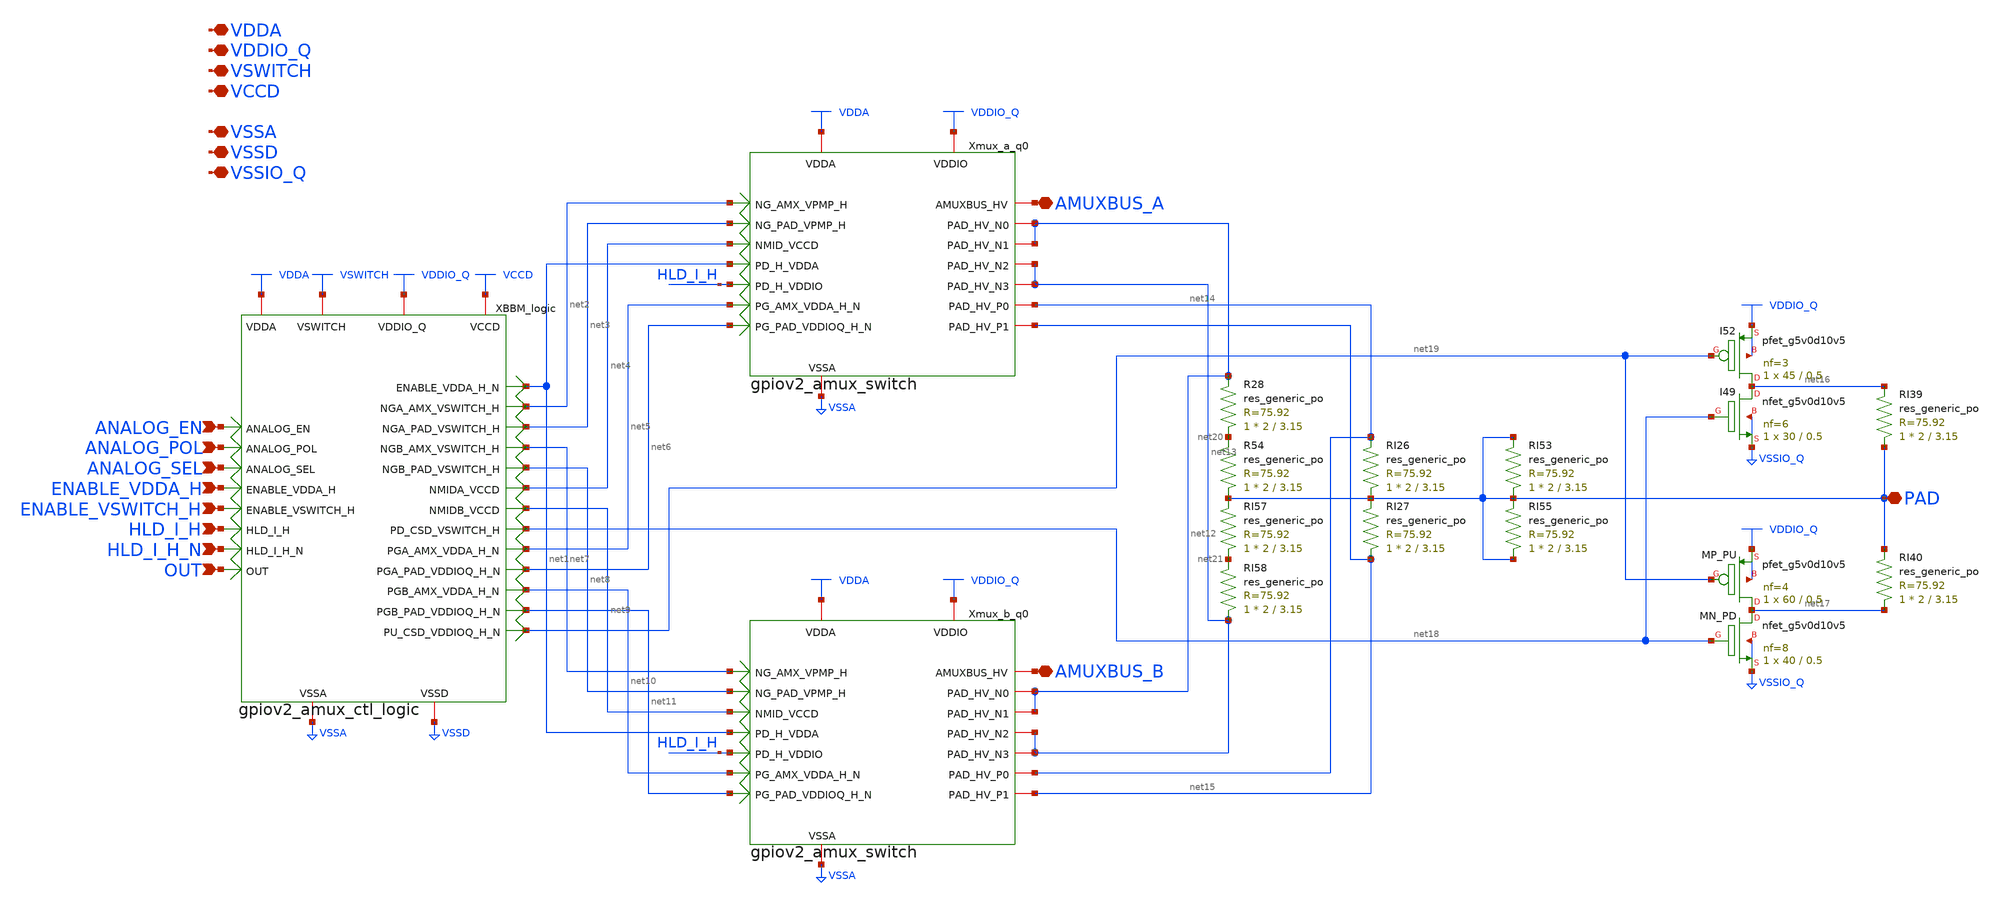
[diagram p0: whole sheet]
** sch_path: gpiov2_amux.sch
* Copyright 2023 David Mitchell Bailey
* Licensed under the Apache License, Version 2.0 (the "License");
* you may not use this file except in compliance with the License.
* You may obtain a copy of the License at
* https://www.apache.org/licenses/LICENSE-2.0
* Unless required by applicable law or agreed to in writing, software
* distributed under the License is distributed on an "AS IS" BASIS,
* WITHOUT WARRANTIES OR CONDITIONS OF ANY KIND, either express or implied.
* See the License for the specific language governing permissions and
* limitations under the License.
**.subckt gpiov2_amux ANALOG_EN ANALOG_POL ANALOG_SEL ENABLE_VDDA_H ENABLE_VSWITCH_H HLD_I_H
*+ HLD_I_H_N OUT AMUXBUS_A AMUXBUS_B PAD VDDA VDDIO_Q VSWITCH VCCD VSSA VSSD VSSIO_Q
*.ipin ANALOG_EN
*.ipin ANALOG_POL
*.ipin ANALOG_SEL
*.ipin ENABLE_VDDA_H
*.ipin ENABLE_VSWITCH_H
*.ipin HLD_I_H
*.ipin HLD_I_H_N
*.ipin OUT
*.iopin AMUXBUS_A
*.iopin AMUXBUS_B
*.iopin PAD
*.iopin VDDA
*.iopin VDDIO_Q
*.iopin VSWITCH
*.iopin VCCD
*.iopin VSSA
*.iopin VSSD
*.iopin VSSIO_Q
XBBM_logic VDDA VSWITCH VDDIO_Q VCCD VSSA ANALOG_POL VSSD ANALOG_SEL net2 net7 net3 net8 net4
+ ANALOG_EN ENABLE_VDDA_H ENABLE_VSWITCH_H net9 HLD_I_H OUT HLD_I_H_N net18 net1 net19 net5 net6 net10 net11
+ gpiov2_amux_ctl_logic
Xmux_a_q0 VDDA VDDIO_Q VSSA net13 net13 AMUXBUS_A net2 net3 HLD_I_H net1 net12 net12 net5 net4 net15
+ net14 net6 gpiov2_amux_switch
Xmux_b_q0 VDDA VDDIO_Q VSSA net13 net13 AMUXBUS_B net7 net8 HLD_I_H net1 net12 net12 net10 net9
+ net15 net14 net11 gpiov2_amux_switch
XRI39 PAD net16 sky130_fd_pr__res_generic_po W=2 L=3.15 m=1
XI49 net16 net18 VSSIO_Q VSSIO_Q sky130_fd_pr__nfet_g5v0d10v5 L=0.5 W=30 nf=6 ad='int((nf+1)/2) * W/nf * 0.29'
+ as='int((nf+2)/2) * W/nf * 0.29' pd='2*int((nf+1)/2) * (W/nf + 0.29)' ps='2*int((nf+2)/2) * (W/nf + 0.29)'
+ nrd='0.29 / W' nrs='0.29 / W' sa=0 sb=0 sd=0 mult=1 m=1
XI52 net16 net19 VDDIO_Q VDDIO_Q sky130_fd_pr__pfet_g5v0d10v5 L=0.5 W=45 nf=3 ad='int((nf+1)/2) * W/nf * 0.29'
+ as='int((nf+2)/2) * W/nf * 0.29' pd='2*int((nf+1)/2) * (W/nf + 0.29)' ps='2*int((nf+2)/2) * (W/nf + 0.29)'
+ nrd='0.29 / W' nrs='0.29 / W' sa=0 sb=0 sd=0 mult=1 m=1
XRI40 net17 PAD sky130_fd_pr__res_generic_po W=2 L=3.15 m=1
XMN_PD net17 net18 VSSIO_Q VSSIO_Q sky130_fd_pr__nfet_g5v0d10v5 L=0.5 W=40 nf=8 ad='int((nf+1)/2) * W/nf * 0.29'
+ as='int((nf+2)/2) * W/nf * 0.29' pd='2*int((nf+1)/2) * (W/nf + 0.29)' ps='2*int((nf+2)/2) * (W/nf + 0.29)'
+ nrd='0.29 / W' nrs='0.29 / W' sa=0 sb=0 sd=0 mult=1 m=1
XMP_PU net17 net19 VDDIO_Q VDDIO_Q sky130_fd_pr__pfet_g5v0d10v5 L=0.5 W=60 nf=4 ad='int((nf+1)/2) * W/nf * 0.29'
+ as='int((nf+2)/2) * W/nf * 0.29' pd='2*int((nf+1)/2) * (W/nf + 0.29)' ps='2*int((nf+2)/2) * (W/nf + 0.29)'
+ nrd='0.29 / W' nrs='0.29 / W' sa=0 sb=0 sd=0 mult=1 m=1
XR54 PAD net20 sky130_fd_pr__res_generic_po W=2 L=3.15 m=1
XR28 net20 net12 sky130_fd_pr__res_generic_po W=2 L=3.15 m=1
XRI58 net13 net21 sky130_fd_pr__res_generic_po W=2 L=3.15 m=1
XRI57 net21 PAD sky130_fd_pr__res_generic_po W=2 L=3.15 m=1
XRI26 PAD net14 sky130_fd_pr__res_generic_po W=2 L=3.15 m=1
XRI27 net15 PAD sky130_fd_pr__res_generic_po W=2 L=3.15 m=1
XRI53 PAD PAD sky130_fd_pr__res_generic_po W=2 L=3.15 m=1
XRI55 PAD PAD sky130_fd_pr__res_generic_po W=2 L=3.15 m=1
**.ends
.end
